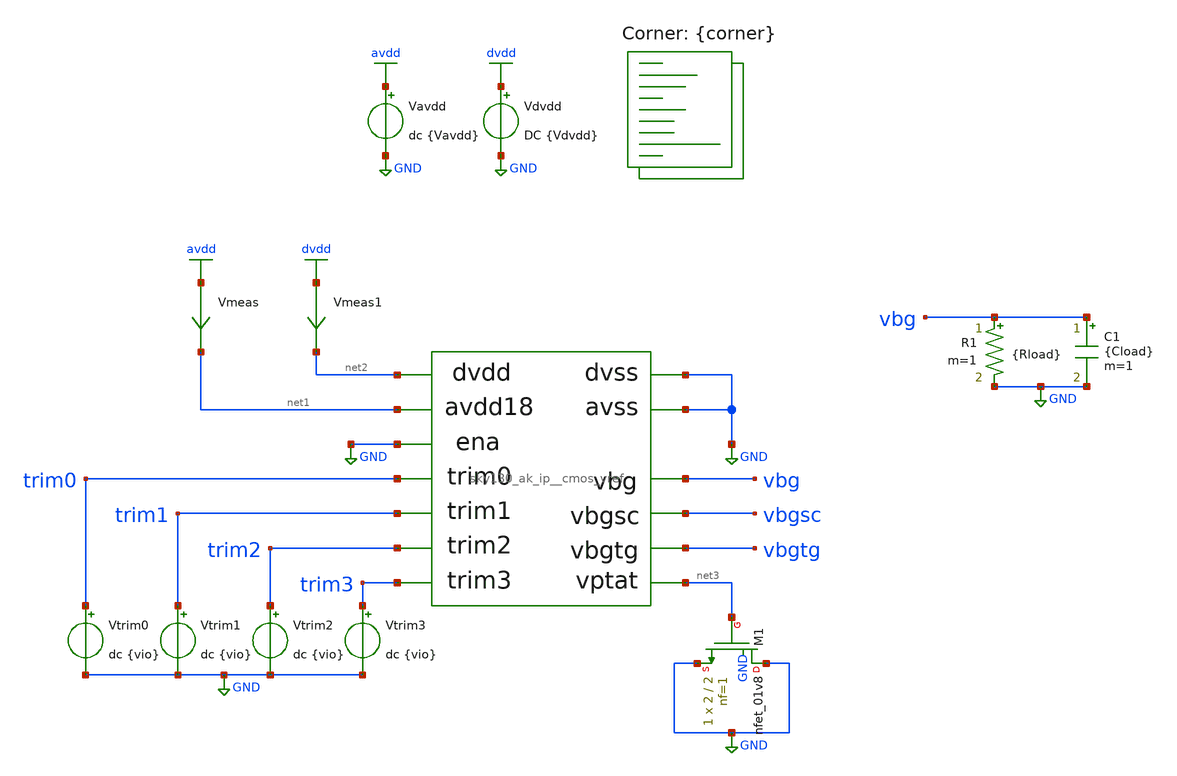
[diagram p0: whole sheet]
** sch_path: cace/templates/tb_trim.sch
**.subckt tb_trim
Vavdd avdd GND dc {Vavdd}
X1 net1 GND trim0 vbg net3 trim1 trim2 trim3 net2 GND GND vbgsc vbgtg sky130_ak_ip__cmos_vref
Vdvdd dvdd GND DC {Vdvdd}
C1 vbg GND {Cload} m=1
R1 vbg GND {Rload} m=1
Vtrim0 trim0 GND dc {vio}
Vmeas avdd net1 0
.save i(vmeas)
Vmeas1 dvdd net2 0
.save i(vmeas1)
Vtrim1 trim1 GND dc {vio}
Vtrim2 trim2 GND dc {vio}
Vtrim3 trim3 GND dc {vio}
XM1 GND net3 GND GND sky130_fd_pr__nfet_01v8 L=2 W=2 nf=1 ad='int((nf+1)/2) * W/nf * 0.29' as='int((nf+2)/2) * W/nf * 0.29'
+ pd='2*int((nf+1)/2) * (W/nf + 0.29)' ps='2*int((nf+2)/2) * (W/nf + 0.29)' nrd='0.29 / W' nrs='0.29 / W'
+ sa=0 sb=0 sd=0 mult=1 m=1
**** begin user architecture code


.option warn=1
.option TEMP={temperature}
.nodeset v(vbg)=1.2
.control
set wr_singlescale
let vref_data = vector(16)
print vref_data
let it = 0
dowhile it < 16
	reset
	save vbg, trim0, trim1, trim2, trim3
	let it_roll=it
	if it_roll%2=1
		alter Vtrim0 0
	end
	let it_roll=floor(it_roll/2)
	if it_roll%2=1
		alter Vtrim1 0
	end
	let it_roll=floor(it_roll/2)
	if it_roll%2=1
		alter Vtrim2 0
	end
	let it_roll=floor(it_roll/2)
	if it_roll%2=1
		alter Vtrim3 0
	end
	print trim0, trim1, trim2, trim3
	op
	let vref_data[it] = V(vbg)
	let it = it + 1
end
print V(vref_data)
let it = 1
setscale 0
wrdata {simpath}/{filename}_{N}.data vref_data[0]
set appendwrite
dowhile it < 16
	setscale it
	wrdata {simpath}/{filename}_{N}.data vref_data[it]
	let it = it + 1
end
quit
.endc


.lib $::SKYWATER_MODELS/sky130.lib.spice {corner}
**** end user architecture code
**.ends
.GLOBAL avdd
.GLOBAL GND
.GLOBAL dvdd
.end
